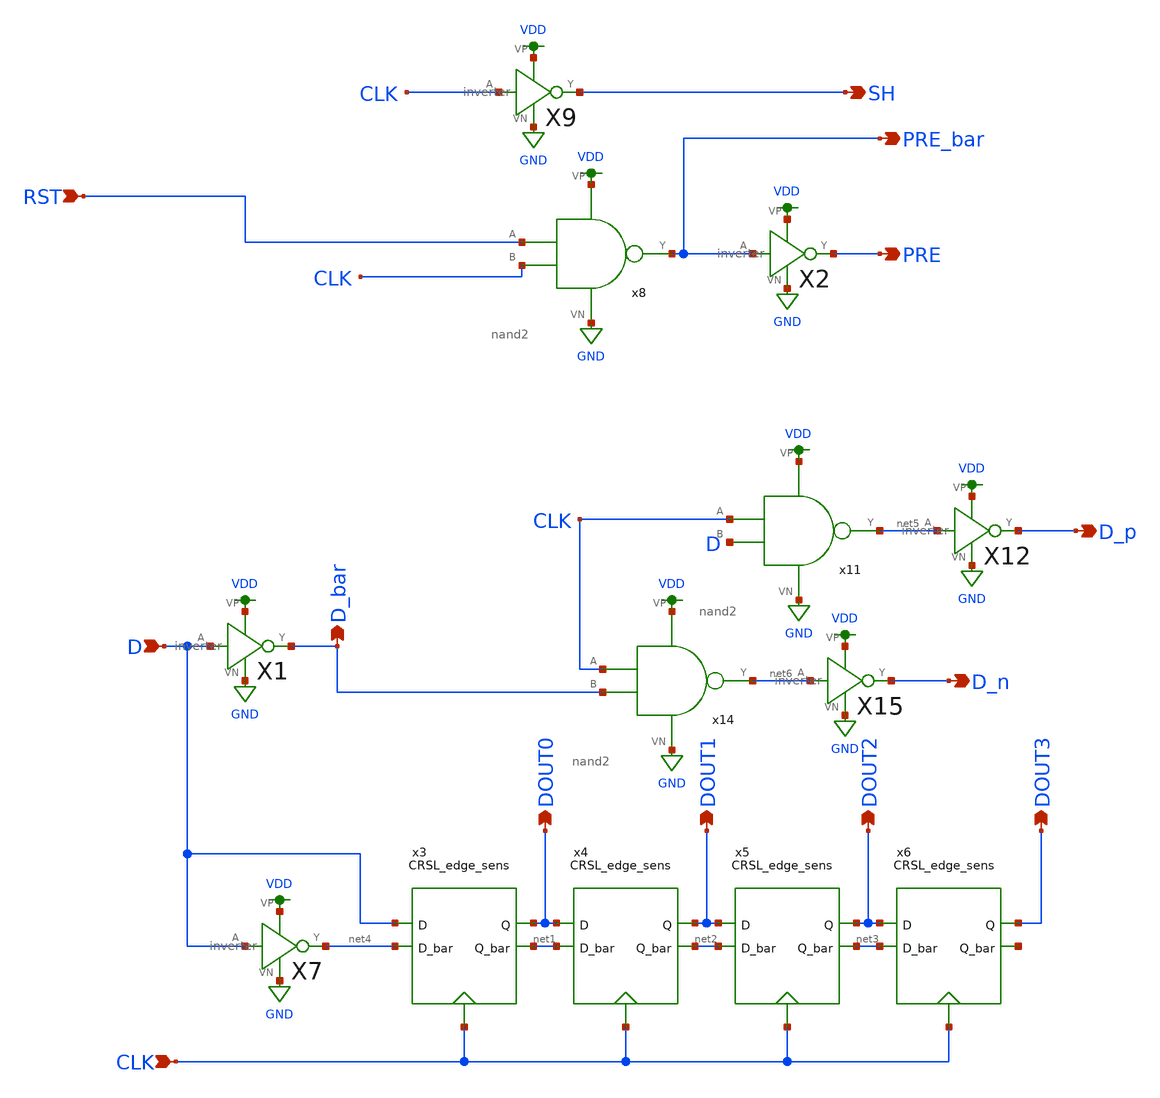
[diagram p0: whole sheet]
** sch_path: schematics/digital_control.sch
**.subckt digital_control D D_bar PRE_bar SH DOUT0 DOUT1 DOUT2 DOUT3 CLK PRE RST D_p D_n
*.ipin D
*.opin D_bar
*.opin PRE_bar
*.opin SH
*.opin DOUT0
*.opin DOUT1
*.opin DOUT2
*.opin DOUT3
*.ipin CLK
*.opin PRE
*.ipin RST
*.opin D_p
*.opin D_n
X2 PRE_bar PRE VDD GND inverter
X9 CLK SH VDD GND inverter
X1 D D_bar VDD GND inverter
X7 D net4 VDD GND inverter
x3 CLK DOUT0 D net1 net4 CRSL_edge_sens
x4 CLK DOUT1 DOUT0 net2 net1 CRSL_edge_sens
x5 CLK DOUT2 DOUT1 net3 net2 CRSL_edge_sens
x6 CLK DOUT3 DOUT2 net7 net3 CRSL_edge_sens
x11 VDD D net5 CLK GND nand2
X12 net5 D_p VDD GND inverter
x14 VDD D_bar net6 CLK GND nand2
X15 net6 D_n VDD GND inverter
x8 VDD CLK PRE_bar RST GND nand2
**.ends

* expanding   symbol:  ../schematics/inverter.sym # of pins=4
** sym_path: schematics/inverter.sym
** sch_path: schematics/inverter.sch
.subckt inverter A Y VP VN
*.ipin A
*.iopin VP
*.iopin VN
*.opin Y
XM1 Y A VP VDD sky130_fd_pr__pfet_01v8 L=0.15 W=1 nf=1 ad='int((nf+1)/2) * W/nf * 0.29' as='int((nf+2)/2) * W/nf * 0.29'
+ pd='2*int((nf+1)/2) * (W/nf + 0.29)' ps='2*int((nf+2)/2) * (W/nf + 0.29)' nrd='0.29 / W' nrs='0.29 / W'
+ sa=0 sb=0 sd=0 mult=1 m=1
XM2 Y A VN GND sky130_fd_pr__nfet_01v8 L=0.15 W=1 nf=1 ad='int((nf+1)/2) * W/nf * 0.29' as='int((nf+2)/2) * W/nf * 0.29'
+ pd='2*int((nf+1)/2) * (W/nf + 0.29)' ps='2*int((nf+2)/2) * (W/nf + 0.29)' nrd='0.29 / W' nrs='0.29 / W'
+ sa=0 sb=0 sd=0 mult=1 m=1
.ends


* expanding   symbol:  ../schematics/CRSL_edge_sens.sym # of pins=5
** sym_path: schematics/CRSL_edge_sens.sym
** sch_path: schematics/CRSL_edge_sens.sch
.subckt CRSL_edge_sens Phi Q D Q_bar D_bar
*.ipin D
*.ipin D_bar
*.opin Q
*.opin Q_bar
*.ipin Phi
XM14 Q_bar Q GND GND sky130_fd_pr__nfet_01v8 L=0.15 W=1 nf=1 ad='int((nf+1)/2) * W/nf * 0.29' as='int((nf+2)/2) * W/nf * 0.29'
+ pd='2*int((nf+1)/2) * (W/nf + 0.29)' ps='2*int((nf+2)/2) * (W/nf + 0.29)' nrd='0.29 / W' nrs='0.29 / W'
+ sa=0 sb=0 sd=0 mult=1 m=1
XM2 Q_bar Phi net3 GND sky130_fd_pr__nfet_01v8 L=0.15 W=1 nf=1 ad='int((nf+1)/2) * W/nf * 0.29' as='int((nf+2)/2) * W/nf * 0.29'
+ pd='2*int((nf+1)/2) * (W/nf + 0.29)' ps='2*int((nf+2)/2) * (W/nf + 0.29)' nrd='0.29 / W' nrs='0.29 / W'
+ sa=0 sb=0 sd=0 mult=1 m=1
XM6 Q Phi net2 GND sky130_fd_pr__nfet_01v8 L=0.15 W=1 nf=1 ad='int((nf+1)/2) * W/nf * 0.29' as='int((nf+2)/2) * W/nf * 0.29'
+ pd='2*int((nf+1)/2) * (W/nf + 0.29)' ps='2*int((nf+2)/2) * (W/nf + 0.29)' nrd='0.29 / W' nrs='0.29 / W'
+ sa=0 sb=0 sd=0 mult=1 m=1
XM7 net4 Phi GND GND sky130_fd_pr__nfet_01v8 L=0.15 W=4 nf=1 ad='int((nf+1)/2) * W/nf * 0.29' as='int((nf+2)/2) * W/nf * 0.29'
+ pd='2*int((nf+1)/2) * (W/nf + 0.29)' ps='2*int((nf+2)/2) * (W/nf + 0.29)' nrd='0.29 / W' nrs='0.29 / W'
+ sa=0 sb=0 sd=0 mult=1 m=1
XM8 net3 net2 net4 GND sky130_fd_pr__nfet_01v8 L=0.15 W=1 nf=1 ad='int((nf+1)/2) * W/nf * 0.29' as='int((nf+2)/2) * W/nf * 0.29'
+ pd='2*int((nf+1)/2) * (W/nf + 0.29)' ps='2*int((nf+2)/2) * (W/nf + 0.29)' nrd='0.29 / W' nrs='0.29 / W'
+ sa=0 sb=0 sd=0 mult=1 m=1
XM12 net3 net2 VDD VDD sky130_fd_pr__pfet_01v8 L=0.15 W=1 nf=1 ad='int((nf+1)/2) * W/nf * 0.29' as='int((nf+2)/2) * W/nf * 0.29'
+ pd='2*int((nf+1)/2) * (W/nf + 0.29)' ps='2*int((nf+2)/2) * (W/nf + 0.29)' nrd='0.29 / W' nrs='0.29 / W'
+ sa=0 sb=0 sd=0 mult=1 m=1
XM9 net2 net3 VDD VDD sky130_fd_pr__pfet_01v8 L=0.15 W=1 nf=1 ad='int((nf+1)/2) * W/nf * 0.29' as='int((nf+2)/2) * W/nf * 0.29'
+ pd='2*int((nf+1)/2) * (W/nf + 0.29)' ps='2*int((nf+2)/2) * (W/nf + 0.29)' nrd='0.29 / W' nrs='0.29 / W'
+ sa=0 sb=0 sd=0 mult=1 m=1
XM1 net1 Phi VDD VDD sky130_fd_pr__pfet_01v8 L=0.15 W=4 nf=1 ad='int((nf+1)/2) * W/nf * 0.29' as='int((nf+2)/2) * W/nf * 0.29'
+ pd='2*int((nf+1)/2) * (W/nf + 0.29)' ps='2*int((nf+2)/2) * (W/nf + 0.29)' nrd='0.29 / W' nrs='0.29 / W'
+ sa=0 sb=0 sd=0 mult=1 m=1
XM3 Q_bar Q net1 VDD sky130_fd_pr__pfet_01v8 L=0.15 W=1 nf=1 ad='int((nf+1)/2) * W/nf * 0.29' as='int((nf+2)/2) * W/nf * 0.29'
+ pd='2*int((nf+1)/2) * (W/nf + 0.29)' ps='2*int((nf+2)/2) * (W/nf + 0.29)' nrd='0.29 / W' nrs='0.29 / W'
+ sa=0 sb=0 sd=0 mult=1 m=1
XM4 Q Q_bar net1 VDD sky130_fd_pr__pfet_01v8 L=0.15 W=1 nf=1 ad='int((nf+1)/2) * W/nf * 0.29' as='int((nf+2)/2) * W/nf * 0.29'
+ pd='2*int((nf+1)/2) * (W/nf + 0.29)' ps='2*int((nf+2)/2) * (W/nf + 0.29)' nrd='0.29 / W' nrs='0.29 / W'
+ sa=0 sb=0 sd=0 mult=1 m=1
XM10 Q Q_bar GND GND sky130_fd_pr__nfet_01v8 L=0.15 W=1 nf=1 ad='int((nf+1)/2) * W/nf * 0.29' as='int((nf+2)/2) * W/nf * 0.29'
+ pd='2*int((nf+1)/2) * (W/nf + 0.29)' ps='2*int((nf+2)/2) * (W/nf + 0.29)' nrd='0.29 / W' nrs='0.29 / W'
+ sa=0 sb=0 sd=0 mult=1 m=1
XM5 net2 net3 net4 GND sky130_fd_pr__nfet_01v8 L=0.15 W=1 nf=1 ad='int((nf+1)/2) * W/nf * 0.29' as='int((nf+2)/2) * W/nf * 0.29'
+ pd='2*int((nf+1)/2) * (W/nf + 0.29)' ps='2*int((nf+2)/2) * (W/nf + 0.29)' nrd='0.29 / W' nrs='0.29 / W'
+ sa=0 sb=0 sd=0 mult=1 m=1
XM11 net3 Phi D_bar VDD sky130_fd_pr__pfet_01v8 L=0.15 W=1 nf=1 ad='int((nf+1)/2) * W/nf * 0.29' as='int((nf+2)/2) * W/nf * 0.29'
+ pd='2*int((nf+1)/2) * (W/nf + 0.29)' ps='2*int((nf+2)/2) * (W/nf + 0.29)' nrd='0.29 / W' nrs='0.29 / W'
+ sa=0 sb=0 sd=0 mult=1 m=1
XM15 net2 Phi D VDD sky130_fd_pr__pfet_01v8 L=0.15 W=1 nf=1 ad='int((nf+1)/2) * W/nf * 0.29' as='int((nf+2)/2) * W/nf * 0.29'
+ pd='2*int((nf+1)/2) * (W/nf + 0.29)' ps='2*int((nf+2)/2) * (W/nf + 0.29)' nrd='0.29 / W' nrs='0.29 / W'
+ sa=0 sb=0 sd=0 mult=1 m=1
.ends


* expanding   symbol:  /home/madvlsi/algorithmic-ada-converter/schematics/nand2.sym # of pins=5
** sym_path: schematics/nand2.sym
** sch_path: schematics/nand2.sch
.subckt nand2 VP B Y A VN
*.iopin VP
*.iopin VN
*.ipin A
*.ipin B
*.opin Y
XM5 Y B VP VP sky130_fd_pr__pfet_01v8 L=0.15 W=1 nf=1 ad='int((nf+1)/2) * W/nf * 0.29' as='int((nf+2)/2) * W/nf * 0.29'
+ pd='2*int((nf+1)/2) * (W/nf + 0.29)' ps='2*int((nf+2)/2) * (W/nf + 0.29)' nrd='0.29 / W' nrs='0.29 / W'
+ sa=0 sb=0 sd=0 mult=1 m=1
XM2 Y A VP VP sky130_fd_pr__pfet_01v8 L=0.15 W=1 nf=1 ad='int((nf+1)/2) * W/nf * 0.29' as='int((nf+2)/2) * W/nf * 0.29'
+ pd='2*int((nf+1)/2) * (W/nf + 0.29)' ps='2*int((nf+2)/2) * (W/nf + 0.29)' nrd='0.29 / W' nrs='0.29 / W'
+ sa=0 sb=0 sd=0 mult=1 m=1
XM1 Y A net1 VN sky130_fd_pr__nfet_01v8 L=0.15 W=1 nf=1 ad='int((nf+1)/2) * W/nf * 0.29' as='int((nf+2)/2) * W/nf * 0.29'
+ pd='2*int((nf+1)/2) * (W/nf + 0.29)' ps='2*int((nf+2)/2) * (W/nf + 0.29)' nrd='0.29 / W' nrs='0.29 / W'
+ sa=0 sb=0 sd=0 mult=1 m=1
XM3 net1 B VN VN sky130_fd_pr__nfet_01v8 L=0.15 W=1 nf=1 ad='int((nf+1)/2) * W/nf * 0.29' as='int((nf+2)/2) * W/nf * 0.29'
+ pd='2*int((nf+1)/2) * (W/nf + 0.29)' ps='2*int((nf+2)/2) * (W/nf + 0.29)' nrd='0.29 / W' nrs='0.29 / W'
+ sa=0 sb=0 sd=0 mult=1 m=1
.ends

.GLOBAL VDD
.GLOBAL GND
.end
